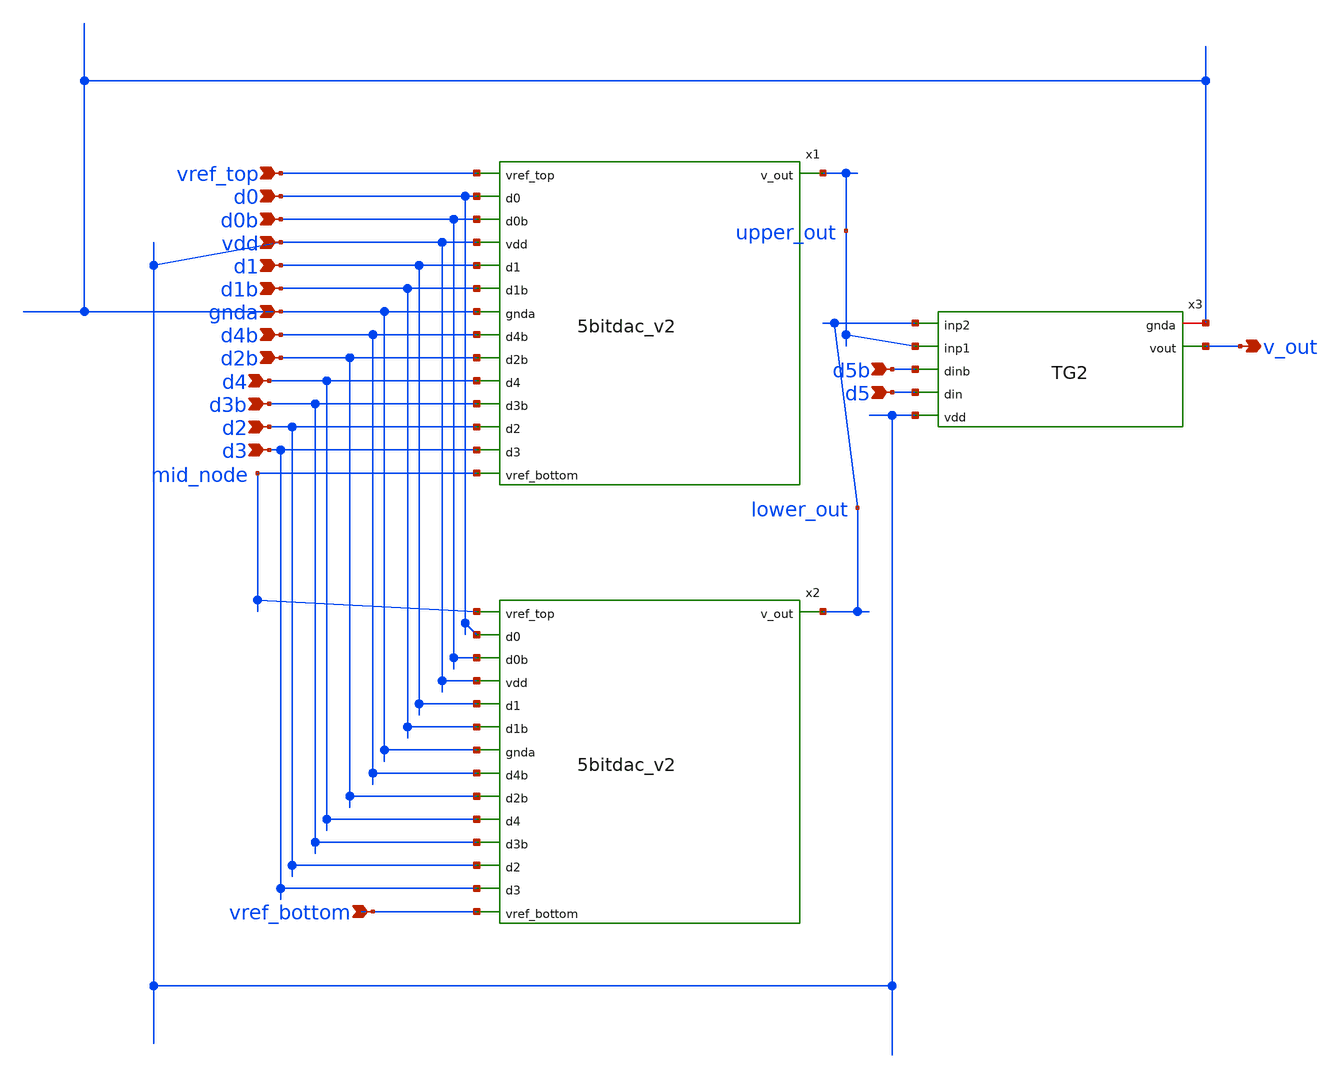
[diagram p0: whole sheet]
** sch_path: prelayout/6bitdac_v2.sch
**.subckt 6bitdac_v2 vref_top d0 d0b vdd d1 d1b d4b d2b d4 d3b gnda d2 d3 d5b d5 v_out vref_bottom
*.ipin vref_top
*.ipin d0
*.ipin d0b
*.ipin vdd
*.ipin d1
*.ipin d1b
*.ipin d4b
*.ipin d2b
*.ipin d4
*.ipin d3b
*.ipin gnda
*.ipin d2
*.ipin d3
*.ipin d5b
*.ipin d5
*.opin v_out
*.ipin vref_bottom
Xx3 gnda v_out lower_out upper_out d5b d5 vdd TG2
x1 vref_top d0 d0b vdd d1 d1b upper_out gnda d4b d2b d4 d3b d2 d3 mid_node 5bitdac_v2
x2 mid_node d0 d0b vdd d1 d1b lower_out gnda d4b d2b d4 d3b d2 d3 vref_bottom 5bitdac_v2
**.ends
.end
